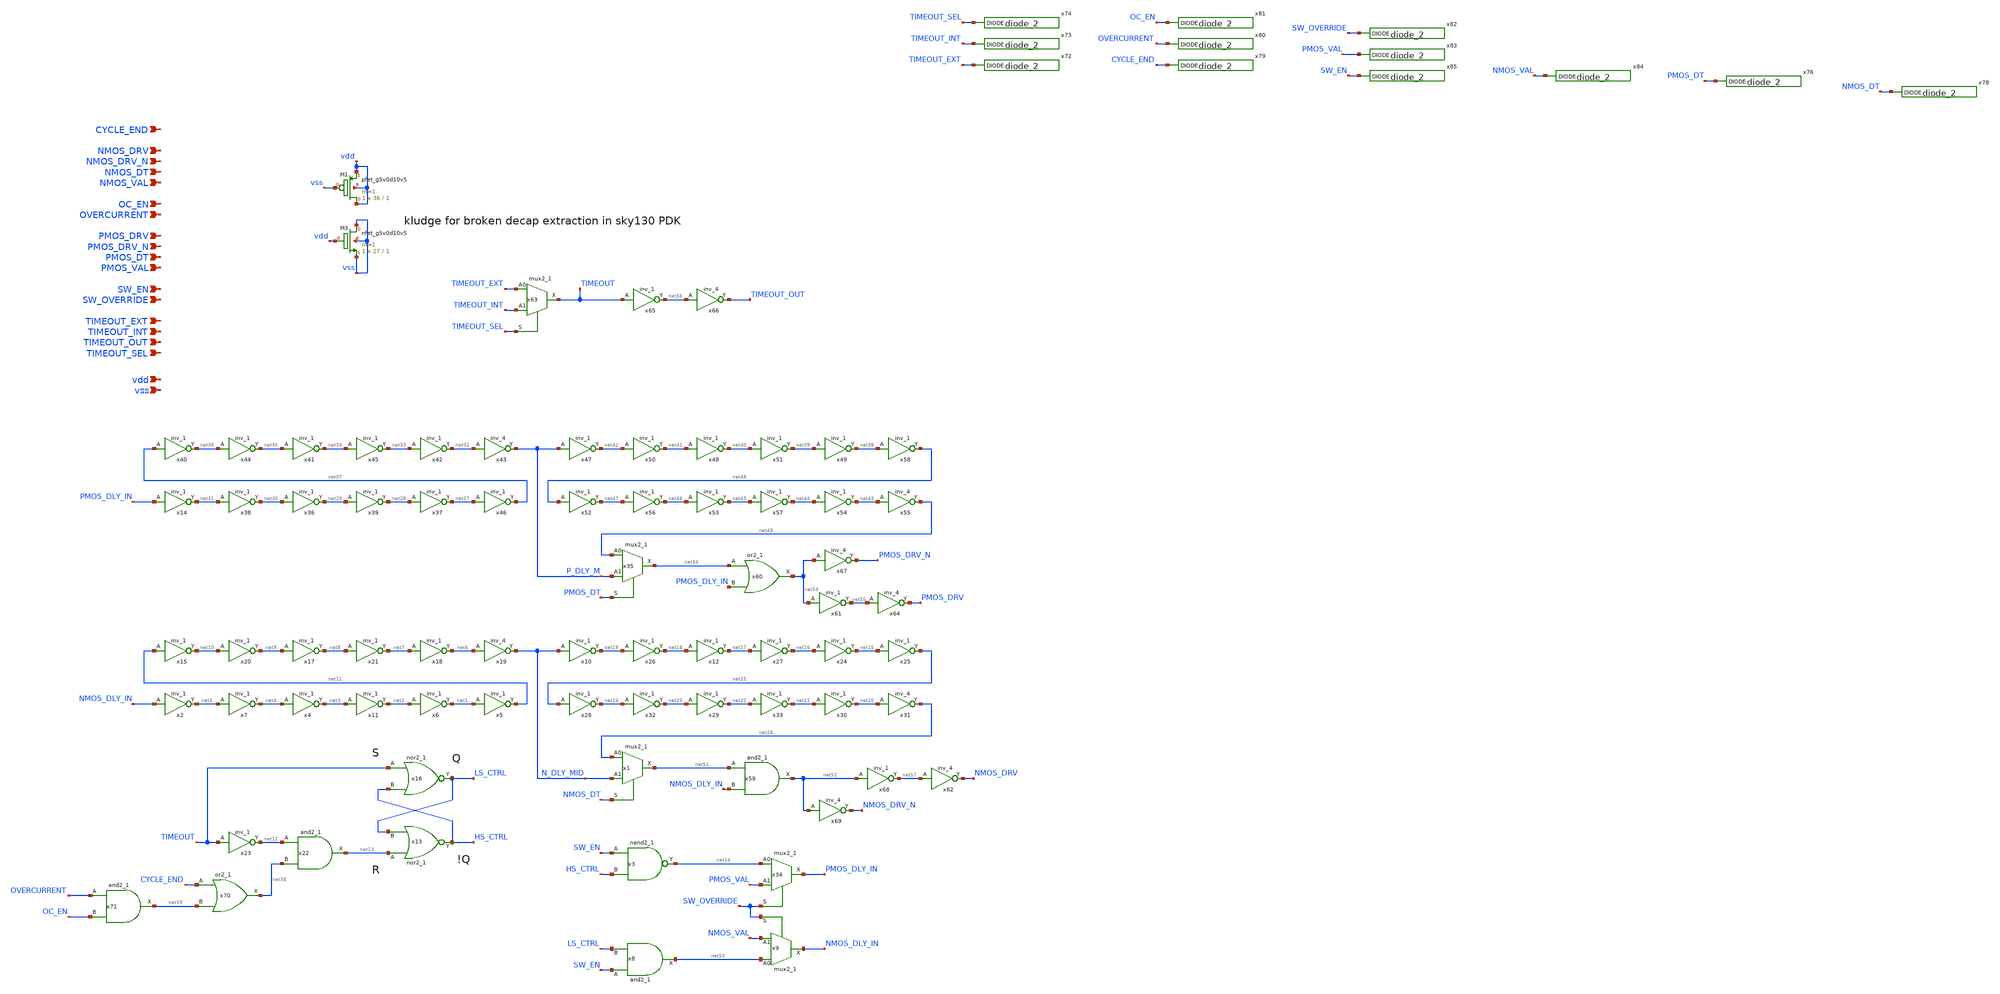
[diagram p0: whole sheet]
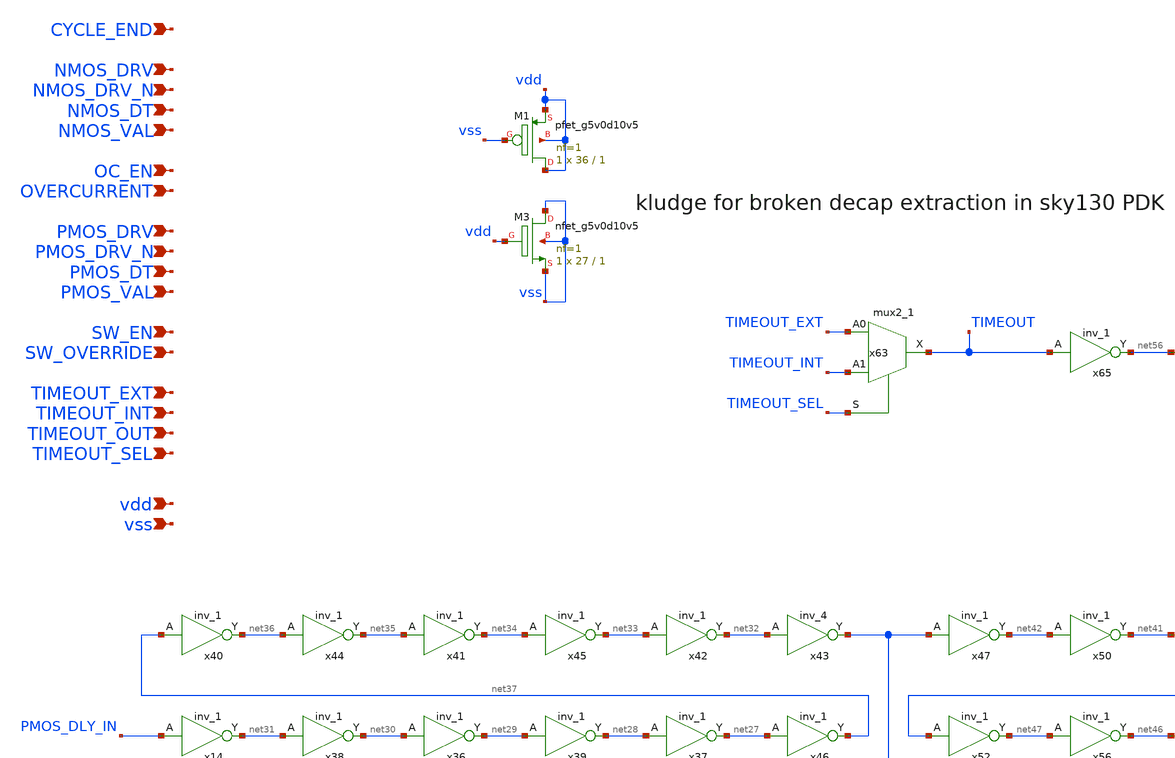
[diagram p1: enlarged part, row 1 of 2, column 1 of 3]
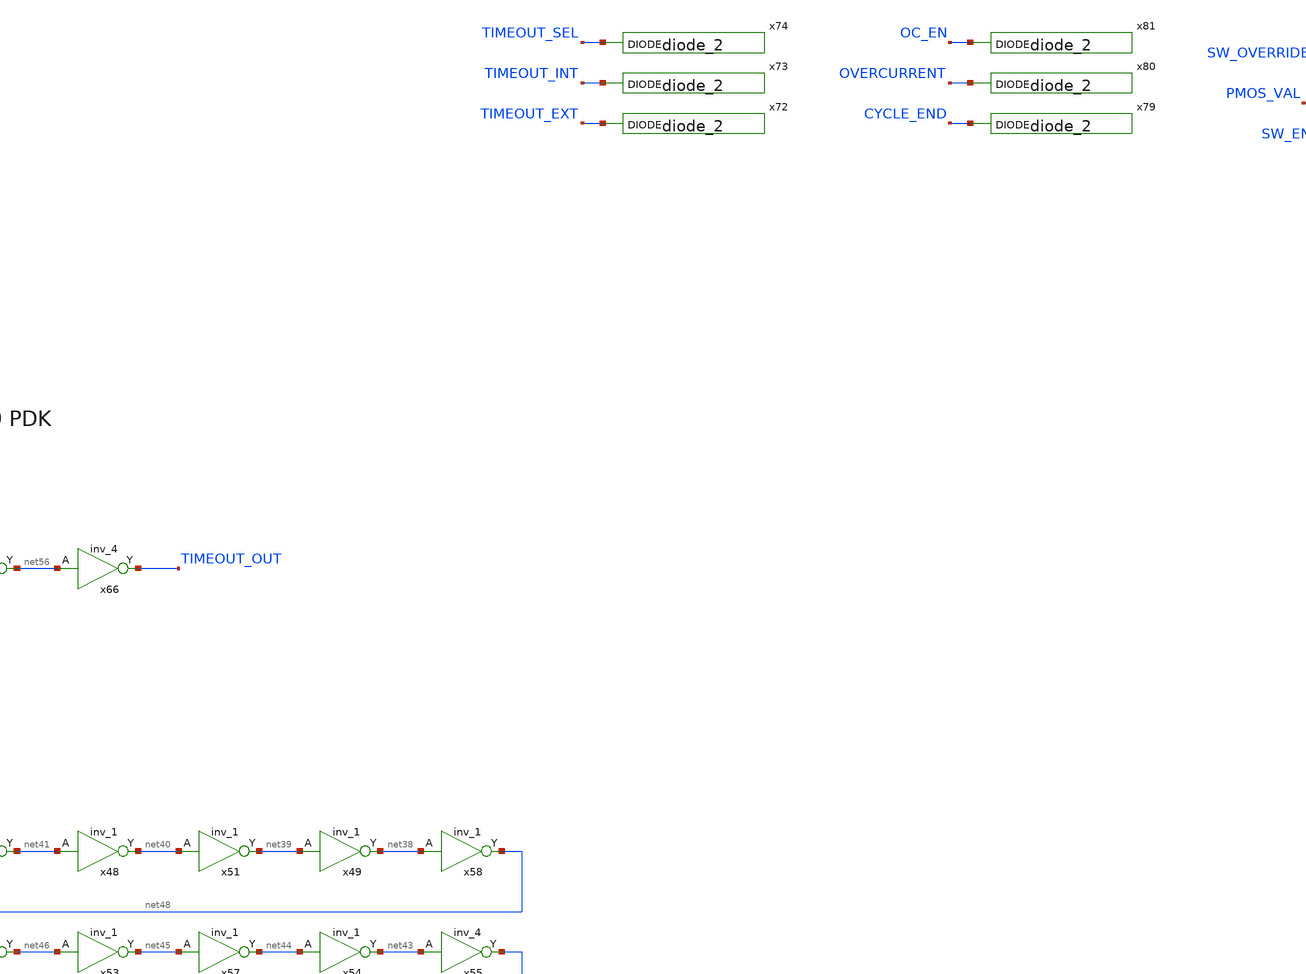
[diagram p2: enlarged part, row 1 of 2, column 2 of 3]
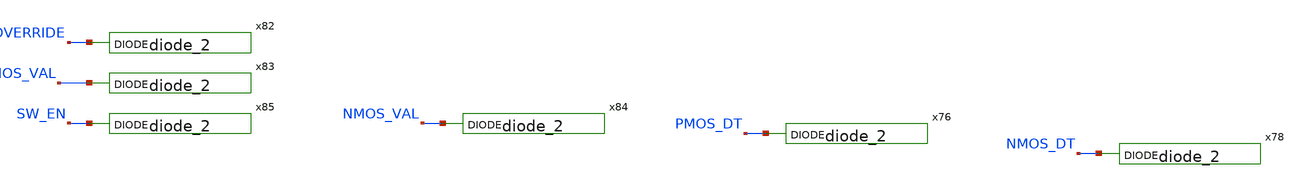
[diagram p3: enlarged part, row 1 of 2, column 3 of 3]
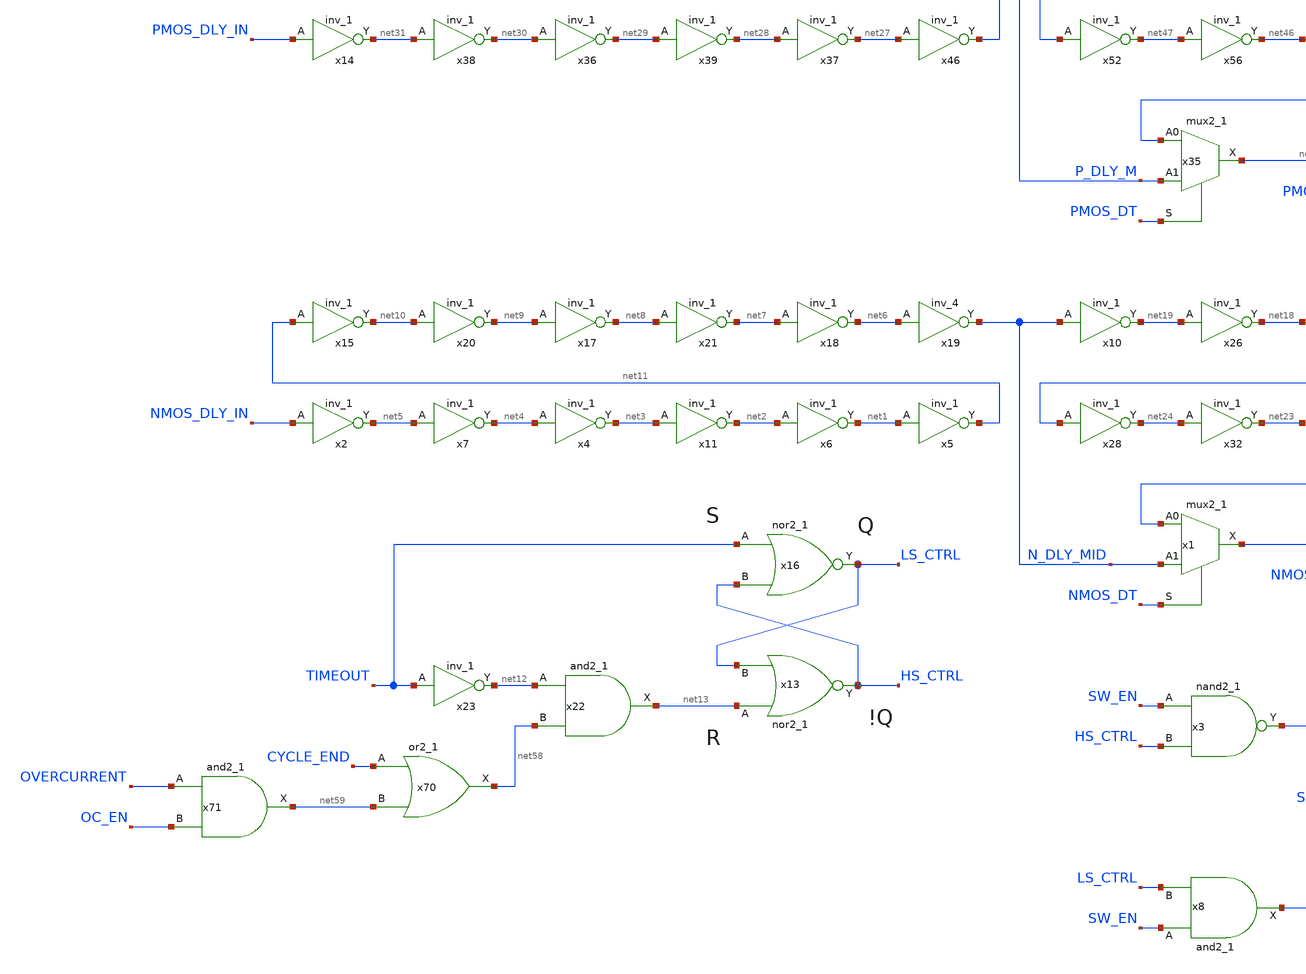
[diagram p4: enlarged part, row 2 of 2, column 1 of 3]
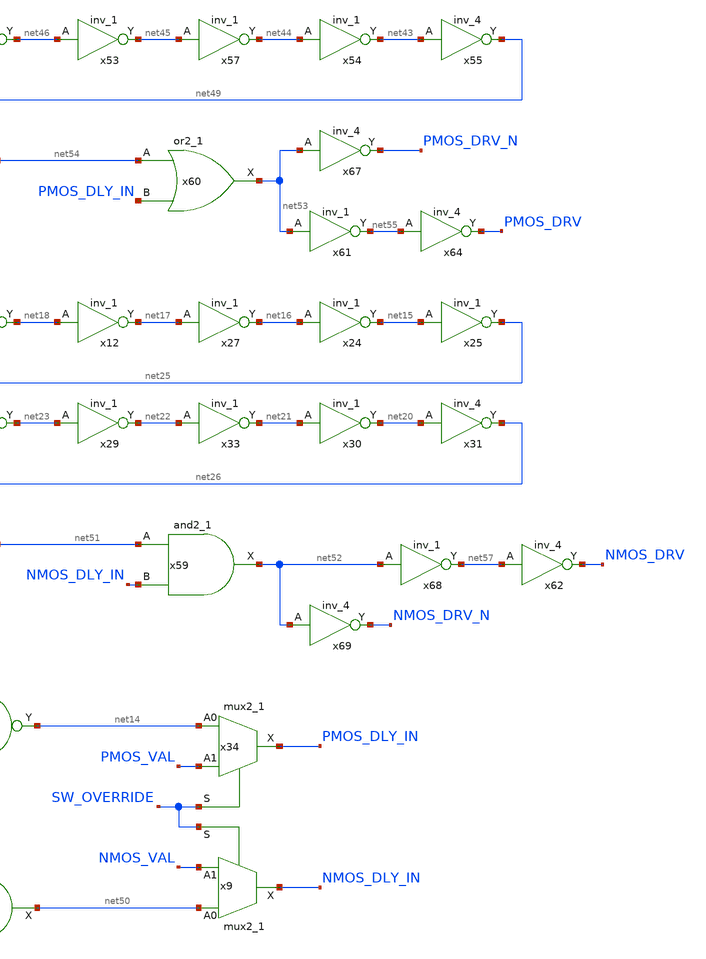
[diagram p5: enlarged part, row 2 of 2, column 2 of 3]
** sch_path: images/foss-asic-tools/addons/examples/Open-PMIC-tapeout/xschem/switch_control.sch
**.subckt switch_control CYCLE_END NMOS_DRV NMOS_DRV_N NMOS_DT NMOS_VAL OC_EN OVERCURRENT PMOS_DRV
*+ PMOS_DRV_N PMOS_DT PMOS_VAL SW_EN SW_OVERRIDE TIMEOUT_EXT TIMEOUT_INT TIMEOUT_OUT TIMEOUT_SEL vdd vss
*.ipin CYCLE_END
*.ipin NMOS_DRV
*.ipin NMOS_DRV_N
*.ipin NMOS_DT
*.ipin NMOS_VAL
*.ipin OC_EN
*.ipin OVERCURRENT
*.ipin PMOS_DRV
*.ipin PMOS_DRV_N
*.ipin PMOS_DT
*.ipin PMOS_VAL
*.ipin SW_EN
*.ipin SW_OVERRIDE
*.ipin TIMEOUT_EXT
*.ipin TIMEOUT_INT
*.ipin TIMEOUT_OUT
*.ipin TIMEOUT_SEL
*.ipin vdd
*.ipin vss
x2 NMOS_DLY_IN vss vss vdd vdd net5 sky130_fd_sc_hvl__inv_1
x18 net7 vss vss vdd vdd net6 sky130_fd_sc_hvl__inv_1
x8 SW_EN LS_CTRL vss vss vdd vdd net50 sky130_fd_sc_hvl__and2_1
x10 N_DLY_MID vss vss vdd vdd net19 sky130_fd_sc_hvl__inv_1
x12 net18 vss vss vdd vdd net17 sky130_fd_sc_hvl__inv_1
x24 net16 vss vss vdd vdd net15 sky130_fd_sc_hvl__inv_1
x26 net19 vss vss vdd vdd net18 sky130_fd_sc_hvl__inv_1
x27 net17 vss vss vdd vdd net16 sky130_fd_sc_hvl__inv_1
x28 net25 vss vss vdd vdd net24 sky130_fd_sc_hvl__inv_1
x29 net23 vss vss vdd vdd net22 sky130_fd_sc_hvl__inv_1
x30 net21 vss vss vdd vdd net20 sky130_fd_sc_hvl__inv_1
x31 net20 vss vss vdd vdd net26 sky130_fd_sc_hvl__inv_4
x32 net24 vss vss vdd vdd net23 sky130_fd_sc_hvl__inv_1
x33 net22 vss vss vdd vdd net21 sky130_fd_sc_hvl__inv_1
x34 net14 PMOS_VAL SW_OVERRIDE vss vss vdd vdd PMOS_DLY_IN sky130_fd_sc_hvl__mux2_1
x25 net15 vss vss vdd vdd net25 sky130_fd_sc_hvl__inv_1
x14 PMOS_DLY_IN vss vss vdd vdd net31 sky130_fd_sc_hvl__inv_1
x35 net49 P_DLY_M PMOS_DT vss vss vdd vdd net54 sky130_fd_sc_hvl__mux2_1
x36 net30 vss vss vdd vdd net29 sky130_fd_sc_hvl__inv_1
x37 net28 vss vss vdd vdd net27 sky130_fd_sc_hvl__inv_1
x38 net31 vss vss vdd vdd net30 sky130_fd_sc_hvl__inv_1
x39 net29 vss vss vdd vdd net28 sky130_fd_sc_hvl__inv_1
x40 net37 vss vss vdd vdd net36 sky130_fd_sc_hvl__inv_1
x41 net35 vss vss vdd vdd net34 sky130_fd_sc_hvl__inv_1
x42 net33 vss vss vdd vdd net32 sky130_fd_sc_hvl__inv_1
x43 net32 vss vss vdd vdd P_DLY_M sky130_fd_sc_hvl__inv_4
x44 net36 vss vss vdd vdd net35 sky130_fd_sc_hvl__inv_1
x45 net34 vss vss vdd vdd net33 sky130_fd_sc_hvl__inv_1
x46 net27 vss vss vdd vdd net37 sky130_fd_sc_hvl__inv_1
x47 P_DLY_M vss vss vdd vdd net42 sky130_fd_sc_hvl__inv_1
x48 net41 vss vss vdd vdd net40 sky130_fd_sc_hvl__inv_1
x49 net39 vss vss vdd vdd net38 sky130_fd_sc_hvl__inv_1
x50 net42 vss vss vdd vdd net41 sky130_fd_sc_hvl__inv_1
x51 net40 vss vss vdd vdd net39 sky130_fd_sc_hvl__inv_1
x52 net48 vss vss vdd vdd net47 sky130_fd_sc_hvl__inv_1
x53 net46 vss vss vdd vdd net45 sky130_fd_sc_hvl__inv_1
x54 net44 vss vss vdd vdd net43 sky130_fd_sc_hvl__inv_1
x55 net43 vss vss vdd vdd net49 sky130_fd_sc_hvl__inv_4
x56 net47 vss vss vdd vdd net46 sky130_fd_sc_hvl__inv_1
x57 net45 vss vss vdd vdd net44 sky130_fd_sc_hvl__inv_1
x58 net38 vss vss vdd vdd net48 sky130_fd_sc_hvl__inv_1
x3 SW_EN HS_CTRL vss vss vdd vdd net14 sky130_fd_sc_hvl__nand2_1
x9 net50 NMOS_VAL SW_OVERRIDE vss vss vdd vdd NMOS_DLY_IN sky130_fd_sc_hvl__mux2_1
x19 net6 vss vss vdd vdd N_DLY_MID sky130_fd_sc_hvl__inv_4
x17 net9 vss vss vdd vdd net8 sky130_fd_sc_hvl__inv_1
x7 net5 vss vss vdd vdd net4 sky130_fd_sc_hvl__inv_1
x1 net26 N_DLY_MID NMOS_DT vss vss vdd vdd net51 sky130_fd_sc_hvl__mux2_1
x15 net11 vss vss vdd vdd net10 sky130_fd_sc_hvl__inv_1
x6 net2 vss vss vdd vdd net1 sky130_fd_sc_hvl__inv_1
x13 net13 LS_CTRL vss vss vdd vdd HS_CTRL sky130_fd_sc_hvl__nor2_1
x16 TIMEOUT HS_CTRL vss vss vdd vdd LS_CTRL sky130_fd_sc_hvl__nor2_1
x59 net51 NMOS_DLY_IN vss vss vdd vdd net52 sky130_fd_sc_hvl__and2_1
x60 net54 PMOS_DLY_IN vss vss vdd vdd net53 sky130_fd_sc_hvl__or2_1
x11 net3 vss vss vdd vdd net2 sky130_fd_sc_hvl__inv_1
x4 net4 vss vss vdd vdd net3 sky130_fd_sc_hvl__inv_1
x61 net53 vss vss vdd vdd net55 sky130_fd_sc_hvl__inv_1
x63 TIMEOUT_EXT TIMEOUT_INT TIMEOUT_SEL vss vss vdd vdd TIMEOUT sky130_fd_sc_hvl__mux2_1
x64 net55 vss vss vdd vdd PMOS_DRV sky130_fd_sc_hvl__inv_4
x20 net10 vss vss vdd vdd net9 sky130_fd_sc_hvl__inv_1
x22 net12 net58 vss vss vdd vdd net13 sky130_fd_sc_hvl__and2_1
x5 net1 vss vss vdd vdd net11 sky130_fd_sc_hvl__inv_1
x65 TIMEOUT vss vss vdd vdd net56 sky130_fd_sc_hvl__inv_1
x66 net56 vss vss vdd vdd TIMEOUT_OUT sky130_fd_sc_hvl__inv_4
x67 net53 vss vss vdd vdd PMOS_DRV_N sky130_fd_sc_hvl__inv_4
x68 net52 vss vss vdd vdd net57 sky130_fd_sc_hvl__inv_1
x69 net52 vss vss vdd vdd NMOS_DRV_N sky130_fd_sc_hvl__inv_4
x62 net57 vss vss vdd vdd NMOS_DRV sky130_fd_sc_hvl__inv_4
x70 CYCLE_END net59 vss vss vdd vdd net58 sky130_fd_sc_hvl__or2_1
x71 OVERCURRENT OC_EN vss vss vdd vdd net59 sky130_fd_sc_hvl__and2_1
x21 net8 vss vss vdd vdd net7 sky130_fd_sc_hvl__inv_1
x23 TIMEOUT vss vss vdd vdd net12 sky130_fd_sc_hvl__inv_1
XM1 vdd vss vdd vdd sky130_fd_pr__pfet_g5v0d10v5 L=1 W=36 nf=1 ad='int((nf+1)/2) * W/nf * 0.29' as='int((nf+2)/2) * W/nf * 0.29'
+ pd='2*int((nf+1)/2) * (W/nf + 0.29)' ps='2*int((nf+2)/2) * (W/nf + 0.29)' nrd='0.29 / W' nrs='0.29 / W'
+ sa=0 sb=0 sd=0 mult=1 m=1
XM3 vss vdd vss vss sky130_fd_pr__nfet_g5v0d10v5 L=1 W=27 nf=1 ad='int((nf+1)/2) * W/nf * 0.29' as='int((nf+2)/2) * W/nf * 0.29'
+ pd='2*int((nf+1)/2) * (W/nf + 0.29)' ps='2*int((nf+2)/2) * (W/nf + 0.29)' nrd='0.29 / W' nrs='0.29 / W'
+ sa=0 sb=0 sd=0 mult=1 m=1
x72 TIMEOUT_EXT vss vss vdd vdd sky130_fd_sc_hvl__diode_2
x73 TIMEOUT_INT vss vss vdd vdd sky130_fd_sc_hvl__diode_2
x74 TIMEOUT_SEL vss vss vdd vdd sky130_fd_sc_hvl__diode_2
x76 PMOS_DT vss vss vdd vdd sky130_fd_sc_hvl__diode_2
x78 NMOS_DT vss vss vdd vdd sky130_fd_sc_hvl__diode_2
x79 CYCLE_END vss vss vdd vdd sky130_fd_sc_hvl__diode_2
x80 OVERCURRENT vss vss vdd vdd sky130_fd_sc_hvl__diode_2
x81 OC_EN vss vss vdd vdd sky130_fd_sc_hvl__diode_2
x82 SW_OVERRIDE vss vss vdd vdd sky130_fd_sc_hvl__diode_2
x83 PMOS_VAL vss vss vdd vdd sky130_fd_sc_hvl__diode_2
x84 NMOS_VAL vss vss vdd vdd sky130_fd_sc_hvl__diode_2
x85 SW_EN vss vss vdd vdd sky130_fd_sc_hvl__diode_2
**** begin user architecture code


.include /usr/share/pdk/sky130A/libs.ref/sky130_fd_sc_hvl/spice/sky130_fd_sc_hvl.spice


**** end user architecture code
**.ends
.end
